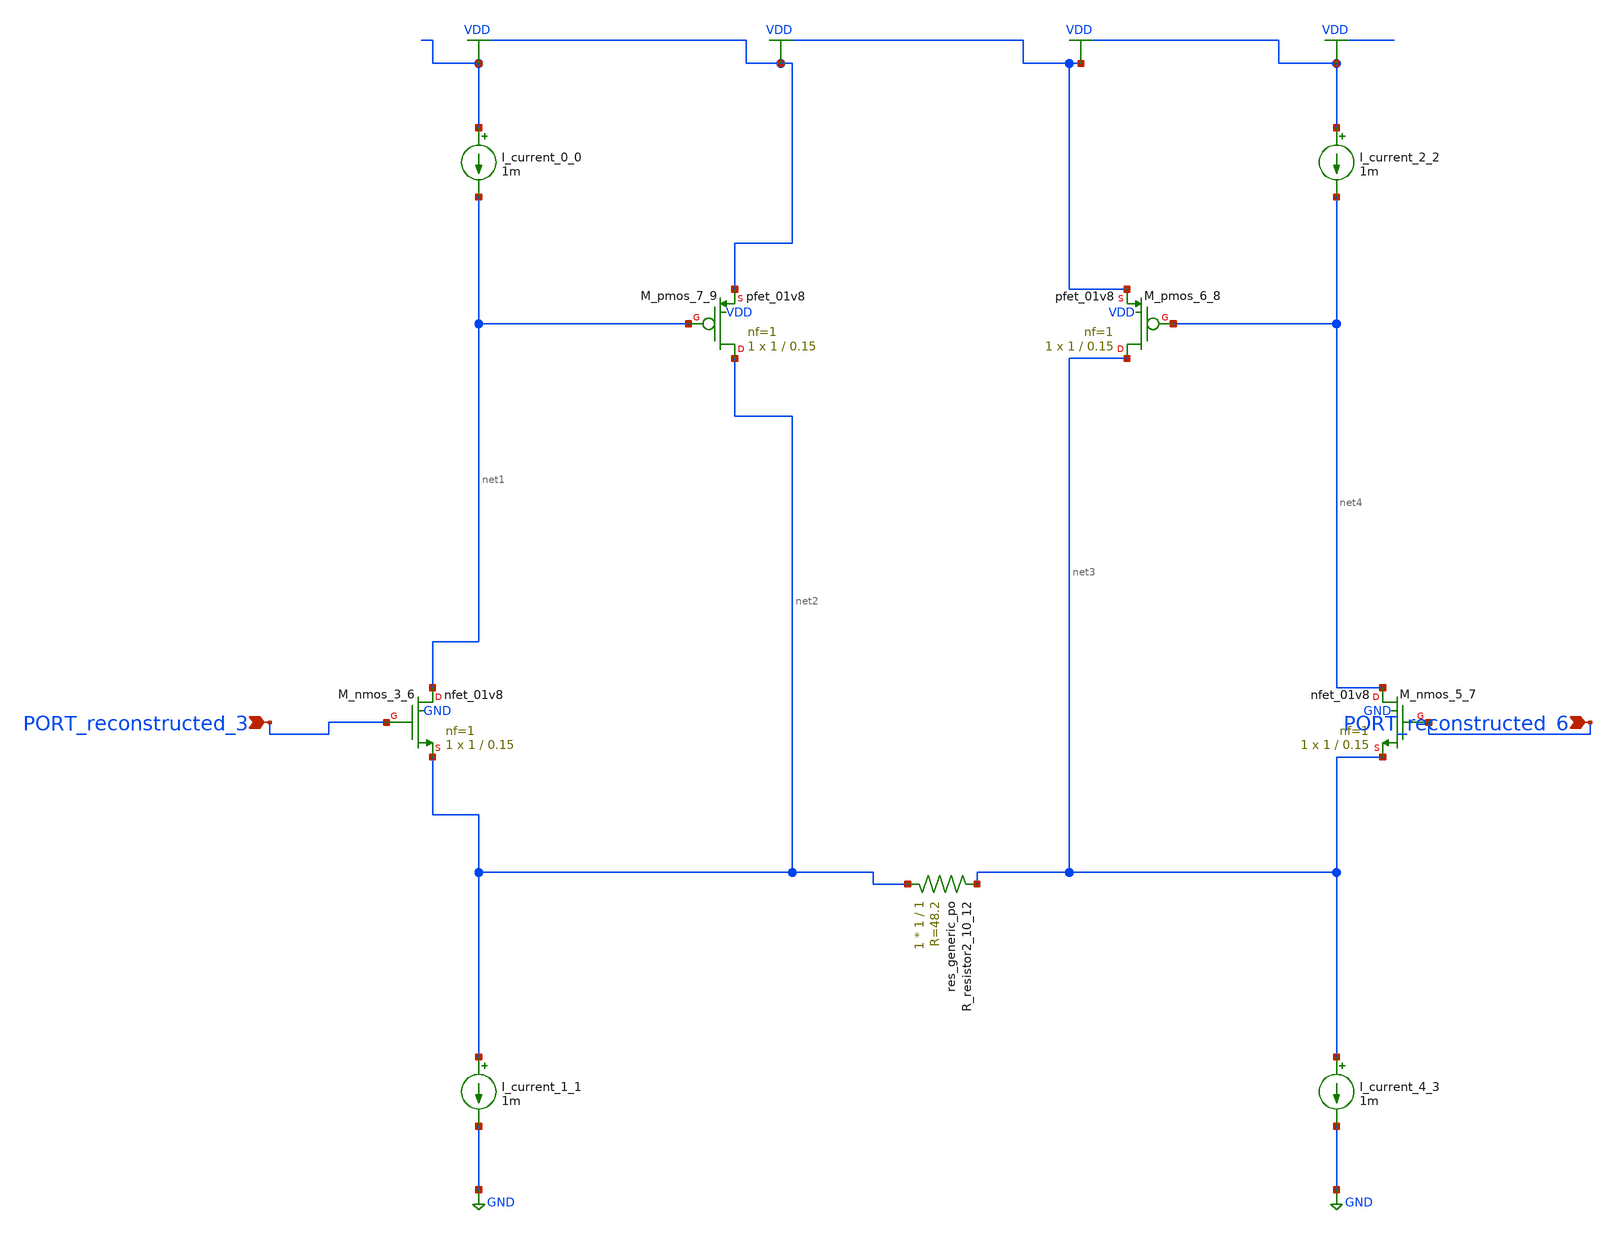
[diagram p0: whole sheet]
** sch_path: schematics/AMSNet/534.sch
**.subckt 534 PORT_reconstructed_6 PORT_reconstructed_3
*.ipin PORT_reconstructed_6
*.ipin PORT_reconstructed_3
I_current_0_0 VDD net1 1m
I_current_1_1 net2 GND 1m
I_current_2_2 VDD net4 1m
I_current_4_3 net3 GND 1m
XM_nmos_3_6 net1 PORT_reconstructed_3 net2 GND sky130_fd_pr__nfet_01v8 L=0.15 W=1 nf=1 ad='int((1 + 1)/2) * 1 / 1 * 0.29'
+ as='int((1 + 2)/2) * 1 / 1 * 0.29' pd='2*int((1 + 1)/2) * (1 / 1 + 0.29)' ps='2*int((1 + 2)/2) * (1 / 1 + 0.29)'
+ nrd='0.29 / 1 ' nrs='0.29 / 1 ' sa=0 sb=0 sd=0 mult=1 m=1
XM_nmos_5_7 net4 PORT_reconstructed_6 net3 GND sky130_fd_pr__nfet_01v8 L=0.15 W=1 nf=1 ad='int((1 + 1)/2) * 1 / 1 * 0.29'
+ as='int((1 + 2)/2) * 1 / 1 * 0.29' pd='2*int((1 + 1)/2) * (1 / 1 + 0.29)' ps='2*int((1 + 2)/2) * (1 / 1 + 0.29)'
+ nrd='0.29 / 1 ' nrs='0.29 / 1 ' sa=0 sb=0 sd=0 mult=1 m=1
XM_pmos_6_8 net3 net4 VDD VDD sky130_fd_pr__pfet_01v8 L=0.15 W=1 nf=1 ad='int((1 + 1)/2) * 1 / 1 * 0.29'
+ as='int((1 + 2)/2) * 1 / 1 * 0.29' pd='2*int((1 + 1)/2) * (1 / 1 + 0.29)' ps='2*int((1 + 2)/2) * (1 / 1 + 0.29)'
+ nrd='0.29 / 1 ' nrs='0.29 / 1 ' sa=0 sb=0 sd=0 mult=1 m=1
XM_pmos_7_9 net2 net1 VDD VDD sky130_fd_pr__pfet_01v8 L=0.15 W=1 nf=1 ad='int((1 + 1)/2) * 1 / 1 * 0.29'
+ as='int((1 + 2)/2) * 1 / 1 * 0.29' pd='2*int((1 + 1)/2) * (1 / 1 + 0.29)' ps='2*int((1 + 2)/2) * (1 / 1 + 0.29)'
+ nrd='0.29 / 1 ' nrs='0.29 / 1 ' sa=0 sb=0 sd=0 mult=1 m=1
XR_resistor2_10_12 net2 net3 sky130_fd_pr__res_generic_po W=1 L=1 m=1
**.ends
.GLOBAL GND
.GLOBAL VDD
.end
